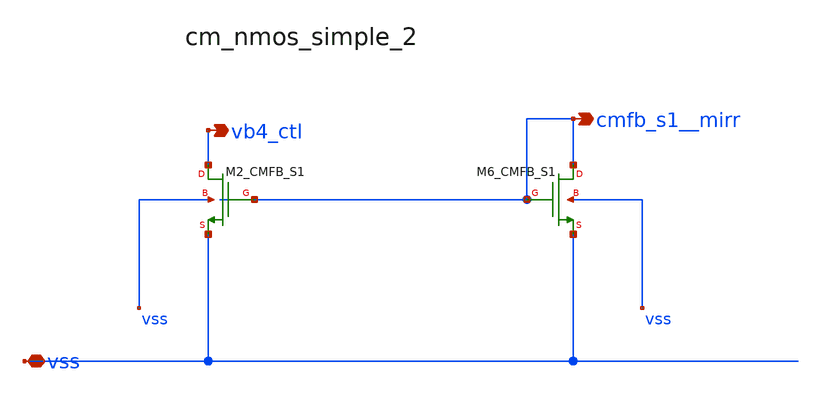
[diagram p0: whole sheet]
** sch_path: analog-db/raw/amp_035_fan_chopper_cmfb_dual/hier/blocks/cm_nmos_simple_2.sch
**.subckt cm_nmos_simple_2 vss vb4_ctl cmfb_s1__mirr
*.iopin vss
*.opin vb4_ctl
*.opin cmfb_s1__mirr
XM2_CMFB_S1 vb4_ctl cmfb_s1__mirr vss vss sg13_lv_nmos w=x_dut_xm2_cmfb_s1_w l=x_dut_xm2_cmfb_s1_l
+ ng=1 m=x_dut_xm2_cmfb_s1_m
XM6_CMFB_S1 cmfb_s1__mirr cmfb_s1__mirr vss vss sg13_lv_nmos w=x_dut_xm6_cmfb_s1_w
+ l=x_dut_xm6_cmfb_s1_l ng=1 m=x_dut_xm6_cmfb_s1_m
**.ends
.end
